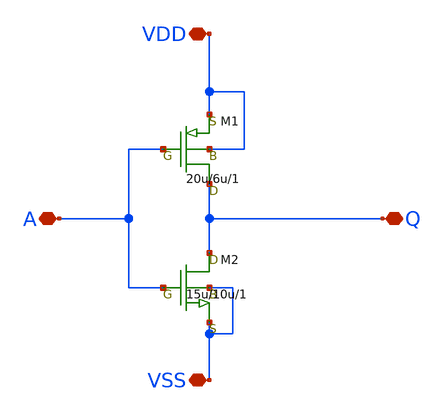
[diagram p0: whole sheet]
** sch_path: Submitted/inverter_elderline.sch
**.subckt inverter_elderline Q A VDD VSS
*.iopin Q
*.iopin A
*.iopin VDD
*.iopin VSS
M1 Q A VDD VDD pch w=20u l=6u as=0 ps=0 ad=0 pd=0 m=1
M2 Q A VSS VSS nch w=15u l=10u as=0 ps=0 ad=0 pd=0 m=1
**.ends
.end
